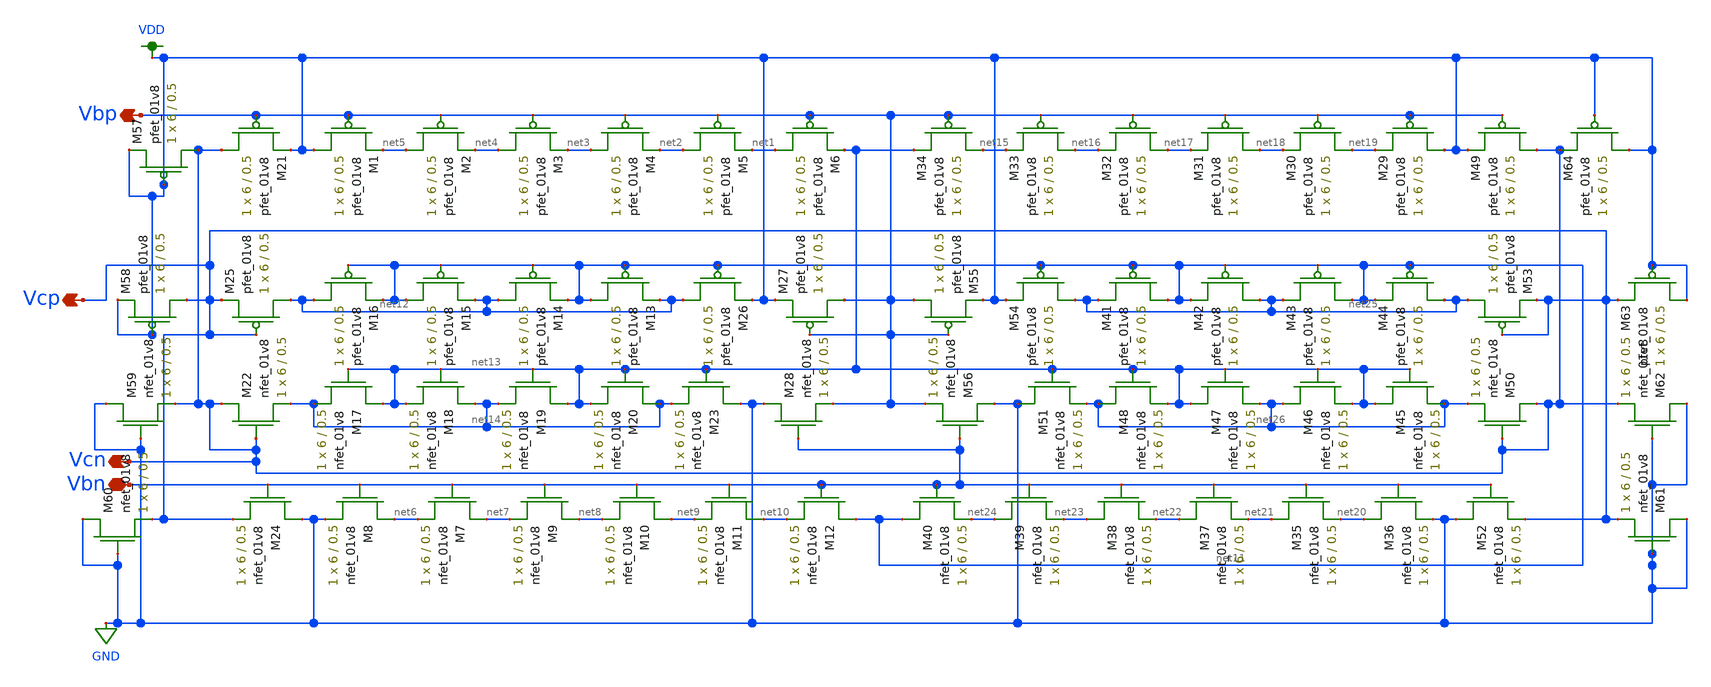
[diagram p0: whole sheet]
** sch_path: mp3/schematic/lds/bias_lvs.sch
**.subckt bias_lvs Vbn Vcn Vcp Vbp
*.iopin Vbn
*.opin Vcn
*.opin Vcp
*.opin Vbp
XM1 VDD Vbp net5 VDD sky130_fd_pr__pfet_01v8 L=0.5 W=6 nf=1 ad='int((nf+1)/2) * W/nf * 0.29' as='int((nf+2)/2) * W/nf * 0.29'
+ pd='2*int((nf+1)/2) * (W/nf + 0.29)' ps='2*int((nf+2)/2) * (W/nf + 0.29)' nrd='0.29 / W' nrs='0.29 / W'
+ sa=0 sb=0 sd=0 mult=1 m=1
XM2 net5 Vbp net4 VDD sky130_fd_pr__pfet_01v8 L=0.5 W=6 nf=1 ad='int((nf+1)/2) * W/nf * 0.29' as='int((nf+2)/2) * W/nf * 0.29'
+ pd='2*int((nf+1)/2) * (W/nf + 0.29)' ps='2*int((nf+2)/2) * (W/nf + 0.29)' nrd='0.29 / W' nrs='0.29 / W'
+ sa=0 sb=0 sd=0 mult=1 m=1
XM3 net4 Vbp net3 VDD sky130_fd_pr__pfet_01v8 L=0.5 W=6 nf=1 ad='int((nf+1)/2) * W/nf * 0.29' as='int((nf+2)/2) * W/nf * 0.29'
+ pd='2*int((nf+1)/2) * (W/nf + 0.29)' ps='2*int((nf+2)/2) * (W/nf + 0.29)' nrd='0.29 / W' nrs='0.29 / W'
+ sa=0 sb=0 sd=0 mult=1 m=1
XM4 net3 Vbp net2 VDD sky130_fd_pr__pfet_01v8 L=0.5 W=6 nf=1 ad='int((nf+1)/2) * W/nf * 0.29' as='int((nf+2)/2) * W/nf * 0.29'
+ pd='2*int((nf+1)/2) * (W/nf + 0.29)' ps='2*int((nf+2)/2) * (W/nf + 0.29)' nrd='0.29 / W' nrs='0.29 / W'
+ sa=0 sb=0 sd=0 mult=1 m=1
XM5 net2 Vbp net1 VDD sky130_fd_pr__pfet_01v8 L=0.5 W=6 nf=1 ad='int((nf+1)/2) * W/nf * 0.29' as='int((nf+2)/2) * W/nf * 0.29'
+ pd='2*int((nf+1)/2) * (W/nf + 0.29)' ps='2*int((nf+2)/2) * (W/nf + 0.29)' nrd='0.29 / W' nrs='0.29 / W'
+ sa=0 sb=0 sd=0 mult=1 m=1
XM6 net1 Vbp net13 VDD sky130_fd_pr__pfet_01v8 L=0.5 W=6 nf=1 ad='int((nf+1)/2) * W/nf * 0.29' as='int((nf+2)/2) * W/nf * 0.29'
+ pd='2*int((nf+1)/2) * (W/nf + 0.29)' ps='2*int((nf+2)/2) * (W/nf + 0.29)' nrd='0.29 / W' nrs='0.29 / W'
+ sa=0 sb=0 sd=0 mult=1 m=1
XM7 net7 Vbn net6 GND sky130_fd_pr__nfet_01v8 L=0.5 W=6 nf=1 ad='int((nf+1)/2) * W/nf * 0.29' as='int((nf+2)/2) * W/nf * 0.29'
+ pd='2*int((nf+1)/2) * (W/nf + 0.29)' ps='2*int((nf+2)/2) * (W/nf + 0.29)' nrd='0.29 / W' nrs='0.29 / W'
+ sa=0 sb=0 sd=0 mult=1 m=1
XM8 net6 Vbn GND GND sky130_fd_pr__nfet_01v8 L=0.5 W=6 nf=1 ad='int((nf+1)/2) * W/nf * 0.29' as='int((nf+2)/2) * W/nf * 0.29'
+ pd='2*int((nf+1)/2) * (W/nf + 0.29)' ps='2*int((nf+2)/2) * (W/nf + 0.29)' nrd='0.29 / W' nrs='0.29 / W'
+ sa=0 sb=0 sd=0 mult=1 m=1
XM9 net8 Vbn net7 GND sky130_fd_pr__nfet_01v8 L=0.5 W=6 nf=1 ad='int((nf+1)/2) * W/nf * 0.29' as='int((nf+2)/2) * W/nf * 0.29'
+ pd='2*int((nf+1)/2) * (W/nf + 0.29)' ps='2*int((nf+2)/2) * (W/nf + 0.29)' nrd='0.29 / W' nrs='0.29 / W'
+ sa=0 sb=0 sd=0 mult=1 m=1
XM10 net9 Vbn net8 GND sky130_fd_pr__nfet_01v8 L=0.5 W=6 nf=1 ad='int((nf+1)/2) * W/nf * 0.29' as='int((nf+2)/2) * W/nf * 0.29'
+ pd='2*int((nf+1)/2) * (W/nf + 0.29)' ps='2*int((nf+2)/2) * (W/nf + 0.29)' nrd='0.29 / W' nrs='0.29 / W'
+ sa=0 sb=0 sd=0 mult=1 m=1
XM11 net10 Vbn net9 GND sky130_fd_pr__nfet_01v8 L=0.5 W=6 nf=1 ad='int((nf+1)/2) * W/nf * 0.29' as='int((nf+2)/2) * W/nf * 0.29'
+ pd='2*int((nf+1)/2) * (W/nf + 0.29)' ps='2*int((nf+2)/2) * (W/nf + 0.29)' nrd='0.29 / W' nrs='0.29 / W'
+ sa=0 sb=0 sd=0 mult=1 m=1
XM12 net11 Vbn net10 GND sky130_fd_pr__nfet_01v8 L=0.5 W=6 nf=1 ad='int((nf+1)/2) * W/nf * 0.29' as='int((nf+2)/2) * W/nf * 0.29'
+ pd='2*int((nf+1)/2) * (W/nf + 0.29)' ps='2*int((nf+2)/2) * (W/nf + 0.29)' nrd='0.29 / W' nrs='0.29 / W'
+ sa=0 sb=0 sd=0 mult=1 m=1
XM13 net11 net11 net12 VDD sky130_fd_pr__pfet_01v8 L=0.5 W=6 nf=1 ad='int((nf+1)/2) * W/nf * 0.29' as='int((nf+2)/2) * W/nf * 0.29'
+ pd='2*int((nf+1)/2) * (W/nf + 0.29)' ps='2*int((nf+2)/2) * (W/nf + 0.29)' nrd='0.29 / W' nrs='0.29 / W'
+ sa=0 sb=0 sd=0 mult=1 m=1
XM14 net12 net11 net11 VDD sky130_fd_pr__pfet_01v8 L=0.5 W=6 nf=1 ad='int((nf+1)/2) * W/nf * 0.29' as='int((nf+2)/2) * W/nf * 0.29'
+ pd='2*int((nf+1)/2) * (W/nf + 0.29)' ps='2*int((nf+2)/2) * (W/nf + 0.29)' nrd='0.29 / W' nrs='0.29 / W'
+ sa=0 sb=0 sd=0 mult=1 m=1
XM15 net11 net11 net12 VDD sky130_fd_pr__pfet_01v8 L=0.5 W=6 nf=1 ad='int((nf+1)/2) * W/nf * 0.29' as='int((nf+2)/2) * W/nf * 0.29'
+ pd='2*int((nf+1)/2) * (W/nf + 0.29)' ps='2*int((nf+2)/2) * (W/nf + 0.29)' nrd='0.29 / W' nrs='0.29 / W'
+ sa=0 sb=0 sd=0 mult=1 m=1
XM16 net12 net11 net11 VDD sky130_fd_pr__pfet_01v8 L=0.5 W=6 nf=1 ad='int((nf+1)/2) * W/nf * 0.29' as='int((nf+2)/2) * W/nf * 0.29'
+ pd='2*int((nf+1)/2) * (W/nf + 0.29)' ps='2*int((nf+2)/2) * (W/nf + 0.29)' nrd='0.29 / W' nrs='0.29 / W'
+ sa=0 sb=0 sd=0 mult=1 m=1
XM17 net13 net13 net14 GND sky130_fd_pr__nfet_01v8 L=0.5 W=6 nf=1 ad='int((nf+1)/2) * W/nf * 0.29' as='int((nf+2)/2) * W/nf * 0.29'
+ pd='2*int((nf+1)/2) * (W/nf + 0.29)' ps='2*int((nf+2)/2) * (W/nf + 0.29)' nrd='0.29 / W' nrs='0.29 / W'
+ sa=0 sb=0 sd=0 mult=1 m=1
XM18 net14 net13 net13 GND sky130_fd_pr__nfet_01v8 L=0.5 W=6 nf=1 ad='int((nf+1)/2) * W/nf * 0.29' as='int((nf+2)/2) * W/nf * 0.29'
+ pd='2*int((nf+1)/2) * (W/nf + 0.29)' ps='2*int((nf+2)/2) * (W/nf + 0.29)' nrd='0.29 / W' nrs='0.29 / W'
+ sa=0 sb=0 sd=0 mult=1 m=1
XM19 net13 net13 net14 GND sky130_fd_pr__nfet_01v8 L=0.5 W=6 nf=1 ad='int((nf+1)/2) * W/nf * 0.29' as='int((nf+2)/2) * W/nf * 0.29'
+ pd='2*int((nf+1)/2) * (W/nf + 0.29)' ps='2*int((nf+2)/2) * (W/nf + 0.29)' nrd='0.29 / W' nrs='0.29 / W'
+ sa=0 sb=0 sd=0 mult=1 m=1
XM20 net14 net13 net13 GND sky130_fd_pr__nfet_01v8 L=0.5 W=6 nf=1 ad='int((nf+1)/2) * W/nf * 0.29' as='int((nf+2)/2) * W/nf * 0.29'
+ pd='2*int((nf+1)/2) * (W/nf + 0.29)' ps='2*int((nf+2)/2) * (W/nf + 0.29)' nrd='0.29 / W' nrs='0.29 / W'
+ sa=0 sb=0 sd=0 mult=1 m=1
XM21 Vcn Vbp VDD VDD sky130_fd_pr__pfet_01v8 L=0.5 W=6 nf=1 ad='int((nf+1)/2) * W/nf * 0.29' as='int((nf+2)/2) * W/nf * 0.29'
+ pd='2*int((nf+1)/2) * (W/nf + 0.29)' ps='2*int((nf+2)/2) * (W/nf + 0.29)' nrd='0.29 / W' nrs='0.29 / W'
+ sa=0 sb=0 sd=0 mult=1 m=1
XM22 Vcn Vcn net14 GND sky130_fd_pr__nfet_01v8 L=0.5 W=6 nf=1 ad='int((nf+1)/2) * W/nf * 0.29' as='int((nf+2)/2) * W/nf * 0.29'
+ pd='2*int((nf+1)/2) * (W/nf + 0.29)' ps='2*int((nf+2)/2) * (W/nf + 0.29)' nrd='0.29 / W' nrs='0.29 / W'
+ sa=0 sb=0 sd=0 mult=1 m=1
XM23 GND net13 net14 GND sky130_fd_pr__nfet_01v8 L=0.5 W=6 nf=1 ad='int((nf+1)/2) * W/nf * 0.29' as='int((nf+2)/2) * W/nf * 0.29'
+ pd='2*int((nf+1)/2) * (W/nf + 0.29)' ps='2*int((nf+2)/2) * (W/nf + 0.29)' nrd='0.29 / W' nrs='0.29 / W'
+ sa=0 sb=0 sd=0 mult=1 m=1
XM24 GND Vbn Vcp GND sky130_fd_pr__nfet_01v8 L=0.5 W=6 nf=1 ad='int((nf+1)/2) * W/nf * 0.29' as='int((nf+2)/2) * W/nf * 0.29'
+ pd='2*int((nf+1)/2) * (W/nf + 0.29)' ps='2*int((nf+2)/2) * (W/nf + 0.29)' nrd='0.29 / W' nrs='0.29 / W'
+ sa=0 sb=0 sd=0 mult=1 m=1
XM25 net12 Vcp Vcp VDD sky130_fd_pr__pfet_01v8 L=0.5 W=6 nf=1 ad='int((nf+1)/2) * W/nf * 0.29' as='int((nf+2)/2) * W/nf * 0.29'
+ pd='2*int((nf+1)/2) * (W/nf + 0.29)' ps='2*int((nf+2)/2) * (W/nf + 0.29)' nrd='0.29 / W' nrs='0.29 / W'
+ sa=0 sb=0 sd=0 mult=1 m=1
XM26 net12 net11 VDD VDD sky130_fd_pr__pfet_01v8 L=0.5 W=6 nf=1 ad='int((nf+1)/2) * W/nf * 0.29' as='int((nf+2)/2) * W/nf * 0.29'
+ pd='2*int((nf+1)/2) * (W/nf + 0.29)' ps='2*int((nf+2)/2) * (W/nf + 0.29)' nrd='0.29 / W' nrs='0.29 / W'
+ sa=0 sb=0 sd=0 mult=1 m=1
XM27 Vbp Vbp VDD VDD sky130_fd_pr__pfet_01v8 L=0.5 W=6 nf=1 ad='int((nf+1)/2) * W/nf * 0.29' as='int((nf+2)/2) * W/nf * 0.29'
+ pd='2*int((nf+1)/2) * (W/nf + 0.29)' ps='2*int((nf+2)/2) * (W/nf + 0.29)' nrd='0.29 / W' nrs='0.29 / W'
+ sa=0 sb=0 sd=0 mult=1 m=1
XM28 GND Vbn Vbp GND sky130_fd_pr__nfet_01v8 L=0.5 W=6 nf=1 ad='int((nf+1)/2) * W/nf * 0.29' as='int((nf+2)/2) * W/nf * 0.29'
+ pd='2*int((nf+1)/2) * (W/nf + 0.29)' ps='2*int((nf+2)/2) * (W/nf + 0.29)' nrd='0.29 / W' nrs='0.29 / W'
+ sa=0 sb=0 sd=0 mult=1 m=1
XM29 VDD Vbp net19 VDD sky130_fd_pr__pfet_01v8 L=0.5 W=6 nf=1 ad='int((nf+1)/2) * W/nf * 0.29' as='int((nf+2)/2) * W/nf * 0.29'
+ pd='2*int((nf+1)/2) * (W/nf + 0.29)' ps='2*int((nf+2)/2) * (W/nf + 0.29)' nrd='0.29 / W' nrs='0.29 / W'
+ sa=0 sb=0 sd=0 mult=1 m=1
XM30 net19 Vbp net18 VDD sky130_fd_pr__pfet_01v8 L=0.5 W=6 nf=1 ad='int((nf+1)/2) * W/nf * 0.29' as='int((nf+2)/2) * W/nf * 0.29'
+ pd='2*int((nf+1)/2) * (W/nf + 0.29)' ps='2*int((nf+2)/2) * (W/nf + 0.29)' nrd='0.29 / W' nrs='0.29 / W'
+ sa=0 sb=0 sd=0 mult=1 m=1
XM31 net18 Vbp net17 VDD sky130_fd_pr__pfet_01v8 L=0.5 W=6 nf=1 ad='int((nf+1)/2) * W/nf * 0.29' as='int((nf+2)/2) * W/nf * 0.29'
+ pd='2*int((nf+1)/2) * (W/nf + 0.29)' ps='2*int((nf+2)/2) * (W/nf + 0.29)' nrd='0.29 / W' nrs='0.29 / W'
+ sa=0 sb=0 sd=0 mult=1 m=1
XM32 net17 Vbp net16 VDD sky130_fd_pr__pfet_01v8 L=0.5 W=6 nf=1 ad='int((nf+1)/2) * W/nf * 0.29' as='int((nf+2)/2) * W/nf * 0.29'
+ pd='2*int((nf+1)/2) * (W/nf + 0.29)' ps='2*int((nf+2)/2) * (W/nf + 0.29)' nrd='0.29 / W' nrs='0.29 / W'
+ sa=0 sb=0 sd=0 mult=1 m=1
XM33 net16 Vbp net15 VDD sky130_fd_pr__pfet_01v8 L=0.5 W=6 nf=1 ad='int((nf+1)/2) * W/nf * 0.29' as='int((nf+2)/2) * W/nf * 0.29'
+ pd='2*int((nf+1)/2) * (W/nf + 0.29)' ps='2*int((nf+2)/2) * (W/nf + 0.29)' nrd='0.29 / W' nrs='0.29 / W'
+ sa=0 sb=0 sd=0 mult=1 m=1
XM34 net15 Vbp net13 VDD sky130_fd_pr__pfet_01v8 L=0.5 W=6 nf=1 ad='int((nf+1)/2) * W/nf * 0.29' as='int((nf+2)/2) * W/nf * 0.29'
+ pd='2*int((nf+1)/2) * (W/nf + 0.29)' ps='2*int((nf+2)/2) * (W/nf + 0.29)' nrd='0.29 / W' nrs='0.29 / W'
+ sa=0 sb=0 sd=0 mult=1 m=1
XM35 net21 Vbn net20 GND sky130_fd_pr__nfet_01v8 L=0.5 W=6 nf=1 ad='int((nf+1)/2) * W/nf * 0.29' as='int((nf+2)/2) * W/nf * 0.29'
+ pd='2*int((nf+1)/2) * (W/nf + 0.29)' ps='2*int((nf+2)/2) * (W/nf + 0.29)' nrd='0.29 / W' nrs='0.29 / W'
+ sa=0 sb=0 sd=0 mult=1 m=1
XM36 net20 Vbn GND GND sky130_fd_pr__nfet_01v8 L=0.5 W=6 nf=1 ad='int((nf+1)/2) * W/nf * 0.29' as='int((nf+2)/2) * W/nf * 0.29'
+ pd='2*int((nf+1)/2) * (W/nf + 0.29)' ps='2*int((nf+2)/2) * (W/nf + 0.29)' nrd='0.29 / W' nrs='0.29 / W'
+ sa=0 sb=0 sd=0 mult=1 m=1
XM37 net22 Vbn net21 GND sky130_fd_pr__nfet_01v8 L=0.5 W=6 nf=1 ad='int((nf+1)/2) * W/nf * 0.29' as='int((nf+2)/2) * W/nf * 0.29'
+ pd='2*int((nf+1)/2) * (W/nf + 0.29)' ps='2*int((nf+2)/2) * (W/nf + 0.29)' nrd='0.29 / W' nrs='0.29 / W'
+ sa=0 sb=0 sd=0 mult=1 m=1
XM38 net23 Vbn net22 GND sky130_fd_pr__nfet_01v8 L=0.5 W=6 nf=1 ad='int((nf+1)/2) * W/nf * 0.29' as='int((nf+2)/2) * W/nf * 0.29'
+ pd='2*int((nf+1)/2) * (W/nf + 0.29)' ps='2*int((nf+2)/2) * (W/nf + 0.29)' nrd='0.29 / W' nrs='0.29 / W'
+ sa=0 sb=0 sd=0 mult=1 m=1
XM39 net24 Vbn net23 GND sky130_fd_pr__nfet_01v8 L=0.5 W=6 nf=1 ad='int((nf+1)/2) * W/nf * 0.29' as='int((nf+2)/2) * W/nf * 0.29'
+ pd='2*int((nf+1)/2) * (W/nf + 0.29)' ps='2*int((nf+2)/2) * (W/nf + 0.29)' nrd='0.29 / W' nrs='0.29 / W'
+ sa=0 sb=0 sd=0 mult=1 m=1
XM40 net11 Vbn net24 GND sky130_fd_pr__nfet_01v8 L=0.5 W=6 nf=1 ad='int((nf+1)/2) * W/nf * 0.29' as='int((nf+2)/2) * W/nf * 0.29'
+ pd='2*int((nf+1)/2) * (W/nf + 0.29)' ps='2*int((nf+2)/2) * (W/nf + 0.29)' nrd='0.29 / W' nrs='0.29 / W'
+ sa=0 sb=0 sd=0 mult=1 m=1
XM41 net11 net11 net25 VDD sky130_fd_pr__pfet_01v8 L=0.5 W=6 nf=1 ad='int((nf+1)/2) * W/nf * 0.29' as='int((nf+2)/2) * W/nf * 0.29'
+ pd='2*int((nf+1)/2) * (W/nf + 0.29)' ps='2*int((nf+2)/2) * (W/nf + 0.29)' nrd='0.29 / W' nrs='0.29 / W'
+ sa=0 sb=0 sd=0 mult=1 m=1
XM42 net25 net11 net11 VDD sky130_fd_pr__pfet_01v8 L=0.5 W=6 nf=1 ad='int((nf+1)/2) * W/nf * 0.29' as='int((nf+2)/2) * W/nf * 0.29'
+ pd='2*int((nf+1)/2) * (W/nf + 0.29)' ps='2*int((nf+2)/2) * (W/nf + 0.29)' nrd='0.29 / W' nrs='0.29 / W'
+ sa=0 sb=0 sd=0 mult=1 m=1
XM43 net11 net11 net25 VDD sky130_fd_pr__pfet_01v8 L=0.5 W=6 nf=1 ad='int((nf+1)/2) * W/nf * 0.29' as='int((nf+2)/2) * W/nf * 0.29'
+ pd='2*int((nf+1)/2) * (W/nf + 0.29)' ps='2*int((nf+2)/2) * (W/nf + 0.29)' nrd='0.29 / W' nrs='0.29 / W'
+ sa=0 sb=0 sd=0 mult=1 m=1
XM44 net25 net11 net11 VDD sky130_fd_pr__pfet_01v8 L=0.5 W=6 nf=1 ad='int((nf+1)/2) * W/nf * 0.29' as='int((nf+2)/2) * W/nf * 0.29'
+ pd='2*int((nf+1)/2) * (W/nf + 0.29)' ps='2*int((nf+2)/2) * (W/nf + 0.29)' nrd='0.29 / W' nrs='0.29 / W'
+ sa=0 sb=0 sd=0 mult=1 m=1
XM45 net13 net13 net26 GND sky130_fd_pr__nfet_01v8 L=0.5 W=6 nf=1 ad='int((nf+1)/2) * W/nf * 0.29' as='int((nf+2)/2) * W/nf * 0.29'
+ pd='2*int((nf+1)/2) * (W/nf + 0.29)' ps='2*int((nf+2)/2) * (W/nf + 0.29)' nrd='0.29 / W' nrs='0.29 / W'
+ sa=0 sb=0 sd=0 mult=1 m=1
XM46 net26 net13 net13 GND sky130_fd_pr__nfet_01v8 L=0.5 W=6 nf=1 ad='int((nf+1)/2) * W/nf * 0.29' as='int((nf+2)/2) * W/nf * 0.29'
+ pd='2*int((nf+1)/2) * (W/nf + 0.29)' ps='2*int((nf+2)/2) * (W/nf + 0.29)' nrd='0.29 / W' nrs='0.29 / W'
+ sa=0 sb=0 sd=0 mult=1 m=1
XM47 net13 net13 net26 GND sky130_fd_pr__nfet_01v8 L=0.5 W=6 nf=1 ad='int((nf+1)/2) * W/nf * 0.29' as='int((nf+2)/2) * W/nf * 0.29'
+ pd='2*int((nf+1)/2) * (W/nf + 0.29)' ps='2*int((nf+2)/2) * (W/nf + 0.29)' nrd='0.29 / W' nrs='0.29 / W'
+ sa=0 sb=0 sd=0 mult=1 m=1
XM48 net26 net13 net13 GND sky130_fd_pr__nfet_01v8 L=0.5 W=6 nf=1 ad='int((nf+1)/2) * W/nf * 0.29' as='int((nf+2)/2) * W/nf * 0.29'
+ pd='2*int((nf+1)/2) * (W/nf + 0.29)' ps='2*int((nf+2)/2) * (W/nf + 0.29)' nrd='0.29 / W' nrs='0.29 / W'
+ sa=0 sb=0 sd=0 mult=1 m=1
XM49 Vcn Vbp VDD VDD sky130_fd_pr__pfet_01v8 L=0.5 W=6 nf=1 ad='int((nf+1)/2) * W/nf * 0.29' as='int((nf+2)/2) * W/nf * 0.29'
+ pd='2*int((nf+1)/2) * (W/nf + 0.29)' ps='2*int((nf+2)/2) * (W/nf + 0.29)' nrd='0.29 / W' nrs='0.29 / W'
+ sa=0 sb=0 sd=0 mult=1 m=1
XM50 Vcn Vcn net26 GND sky130_fd_pr__nfet_01v8 L=0.5 W=6 nf=1 ad='int((nf+1)/2) * W/nf * 0.29' as='int((nf+2)/2) * W/nf * 0.29'
+ pd='2*int((nf+1)/2) * (W/nf + 0.29)' ps='2*int((nf+2)/2) * (W/nf + 0.29)' nrd='0.29 / W' nrs='0.29 / W'
+ sa=0 sb=0 sd=0 mult=1 m=1
XM51 GND net13 net26 GND sky130_fd_pr__nfet_01v8 L=0.5 W=6 nf=1 ad='int((nf+1)/2) * W/nf * 0.29' as='int((nf+2)/2) * W/nf * 0.29'
+ pd='2*int((nf+1)/2) * (W/nf + 0.29)' ps='2*int((nf+2)/2) * (W/nf + 0.29)' nrd='0.29 / W' nrs='0.29 / W'
+ sa=0 sb=0 sd=0 mult=1 m=1
XM52 GND Vbn Vcp GND sky130_fd_pr__nfet_01v8 L=0.5 W=6 nf=1 ad='int((nf+1)/2) * W/nf * 0.29' as='int((nf+2)/2) * W/nf * 0.29'
+ pd='2*int((nf+1)/2) * (W/nf + 0.29)' ps='2*int((nf+2)/2) * (W/nf + 0.29)' nrd='0.29 / W' nrs='0.29 / W'
+ sa=0 sb=0 sd=0 mult=1 m=1
XM53 net25 Vcp Vcp VDD sky130_fd_pr__pfet_01v8 L=0.5 W=6 nf=1 ad='int((nf+1)/2) * W/nf * 0.29' as='int((nf+2)/2) * W/nf * 0.29'
+ pd='2*int((nf+1)/2) * (W/nf + 0.29)' ps='2*int((nf+2)/2) * (W/nf + 0.29)' nrd='0.29 / W' nrs='0.29 / W'
+ sa=0 sb=0 sd=0 mult=1 m=1
XM54 net25 net11 VDD VDD sky130_fd_pr__pfet_01v8 L=0.5 W=6 nf=1 ad='int((nf+1)/2) * W/nf * 0.29' as='int((nf+2)/2) * W/nf * 0.29'
+ pd='2*int((nf+1)/2) * (W/nf + 0.29)' ps='2*int((nf+2)/2) * (W/nf + 0.29)' nrd='0.29 / W' nrs='0.29 / W'
+ sa=0 sb=0 sd=0 mult=1 m=1
XM55 Vbp Vbp VDD VDD sky130_fd_pr__pfet_01v8 L=0.5 W=6 nf=1 ad='int((nf+1)/2) * W/nf * 0.29' as='int((nf+2)/2) * W/nf * 0.29'
+ pd='2*int((nf+1)/2) * (W/nf + 0.29)' ps='2*int((nf+2)/2) * (W/nf + 0.29)' nrd='0.29 / W' nrs='0.29 / W'
+ sa=0 sb=0 sd=0 mult=1 m=1
XM56 GND Vbn Vbp GND sky130_fd_pr__nfet_01v8 L=0.5 W=6 nf=1 ad='int((nf+1)/2) * W/nf * 0.29' as='int((nf+2)/2) * W/nf * 0.29'
+ pd='2*int((nf+1)/2) * (W/nf + 0.29)' ps='2*int((nf+2)/2) * (W/nf + 0.29)' nrd='0.29 / W' nrs='0.29 / W'
+ sa=0 sb=0 sd=0 mult=1 m=1
XM57 Vcn VDD VDD VDD sky130_fd_pr__pfet_01v8 L=0.5 W=6 nf=1 ad='int((nf+1)/2) * W/nf * 0.29' as='int((nf+2)/2) * W/nf * 0.29'
+ pd='2*int((nf+1)/2) * (W/nf + 0.29)' ps='2*int((nf+2)/2) * (W/nf + 0.29)' nrd='0.29 / W' nrs='0.29 / W'
+ sa=0 sb=0 sd=0 mult=1 m=1
XM58 Vcp VDD VDD VDD sky130_fd_pr__pfet_01v8 L=0.5 W=6 nf=1 ad='int((nf+1)/2) * W/nf * 0.29' as='int((nf+2)/2) * W/nf * 0.29'
+ pd='2*int((nf+1)/2) * (W/nf + 0.29)' ps='2*int((nf+2)/2) * (W/nf + 0.29)' nrd='0.29 / W' nrs='0.29 / W'
+ sa=0 sb=0 sd=0 mult=1 m=1
XM59 GND GND Vcn GND sky130_fd_pr__nfet_01v8 L=0.5 W=6 nf=1 ad='int((nf+1)/2) * W/nf * 0.29' as='int((nf+2)/2) * W/nf * 0.29'
+ pd='2*int((nf+1)/2) * (W/nf + 0.29)' ps='2*int((nf+2)/2) * (W/nf + 0.29)' nrd='0.29 / W' nrs='0.29 / W'
+ sa=0 sb=0 sd=0 mult=1 m=1
XM60 GND GND Vcp GND sky130_fd_pr__nfet_01v8 L=0.5 W=6 nf=1 ad='int((nf+1)/2) * W/nf * 0.29' as='int((nf+2)/2) * W/nf * 0.29'
+ pd='2*int((nf+1)/2) * (W/nf + 0.29)' ps='2*int((nf+2)/2) * (W/nf + 0.29)' nrd='0.29 / W' nrs='0.29 / W'
+ sa=0 sb=0 sd=0 mult=1 m=1
XM61 GND GND Vcp GND sky130_fd_pr__nfet_01v8 L=0.5 W=6 nf=1 ad='int((nf+1)/2) * W/nf * 0.29' as='int((nf+2)/2) * W/nf * 0.29'
+ pd='2*int((nf+1)/2) * (W/nf + 0.29)' ps='2*int((nf+2)/2) * (W/nf + 0.29)' nrd='0.29 / W' nrs='0.29 / W'
+ sa=0 sb=0 sd=0 mult=1 m=1
XM62 GND GND Vcn GND sky130_fd_pr__nfet_01v8 L=0.5 W=6 nf=1 ad='int((nf+1)/2) * W/nf * 0.29' as='int((nf+2)/2) * W/nf * 0.29'
+ pd='2*int((nf+1)/2) * (W/nf + 0.29)' ps='2*int((nf+2)/2) * (W/nf + 0.29)' nrd='0.29 / W' nrs='0.29 / W'
+ sa=0 sb=0 sd=0 mult=1 m=1
XM63 VDD VDD Vcp VDD sky130_fd_pr__pfet_01v8 L=0.5 W=6 nf=1 ad='int((nf+1)/2) * W/nf * 0.29' as='int((nf+2)/2) * W/nf * 0.29'
+ pd='2*int((nf+1)/2) * (W/nf + 0.29)' ps='2*int((nf+2)/2) * (W/nf + 0.29)' nrd='0.29 / W' nrs='0.29 / W'
+ sa=0 sb=0 sd=0 mult=1 m=1
XM64 VDD VDD Vcn VDD sky130_fd_pr__pfet_01v8 L=0.5 W=6 nf=1 ad='int((nf+1)/2) * W/nf * 0.29' as='int((nf+2)/2) * W/nf * 0.29'
+ pd='2*int((nf+1)/2) * (W/nf + 0.29)' ps='2*int((nf+2)/2) * (W/nf + 0.29)' nrd='0.29 / W' nrs='0.29 / W'
+ sa=0 sb=0 sd=0 mult=1 m=1
**.ends
.GLOBAL VDD
.GLOBAL GND
.end
